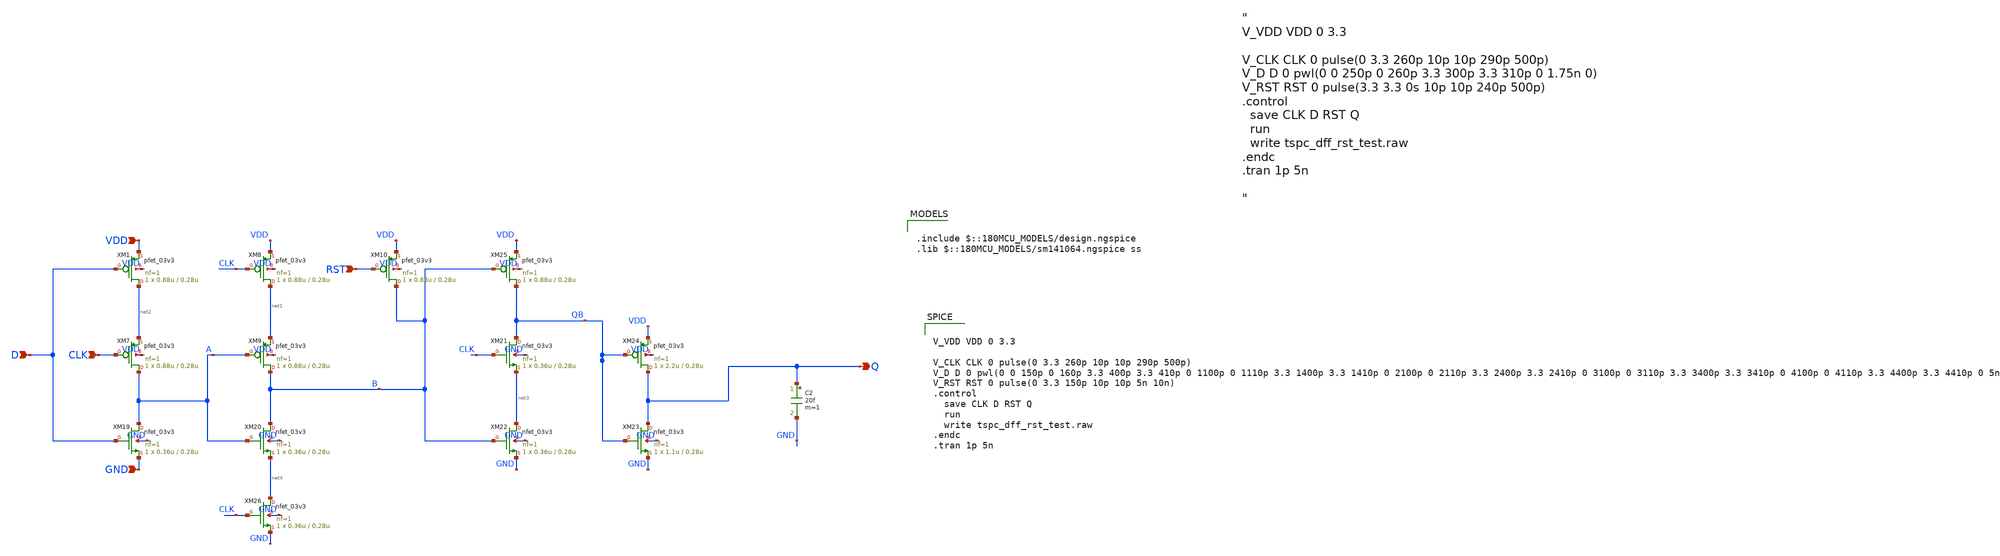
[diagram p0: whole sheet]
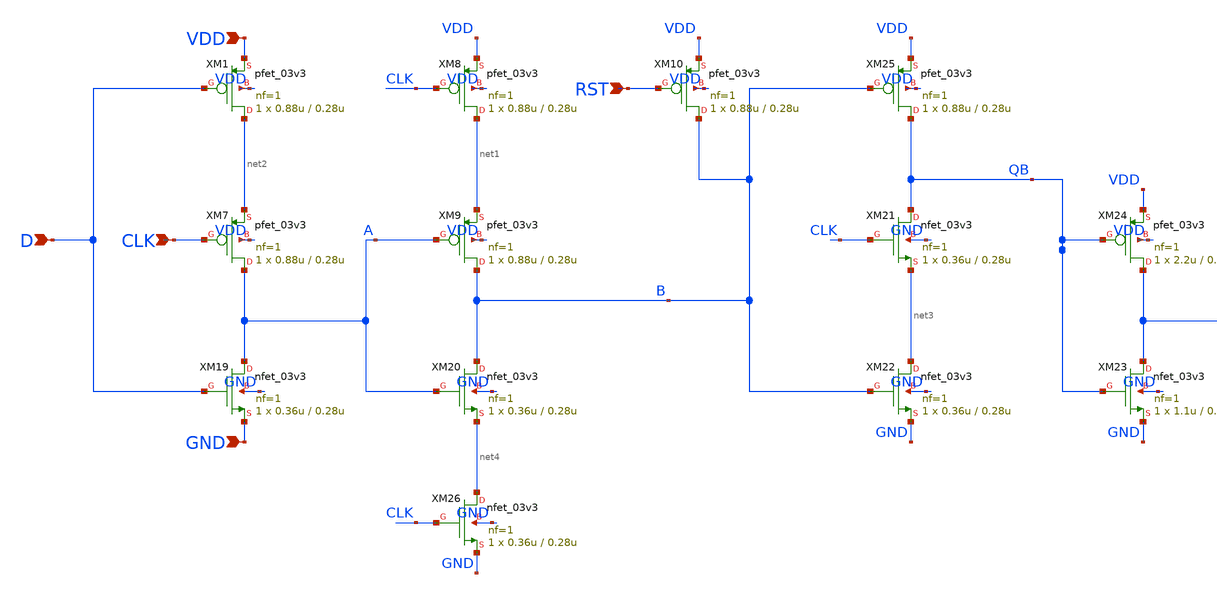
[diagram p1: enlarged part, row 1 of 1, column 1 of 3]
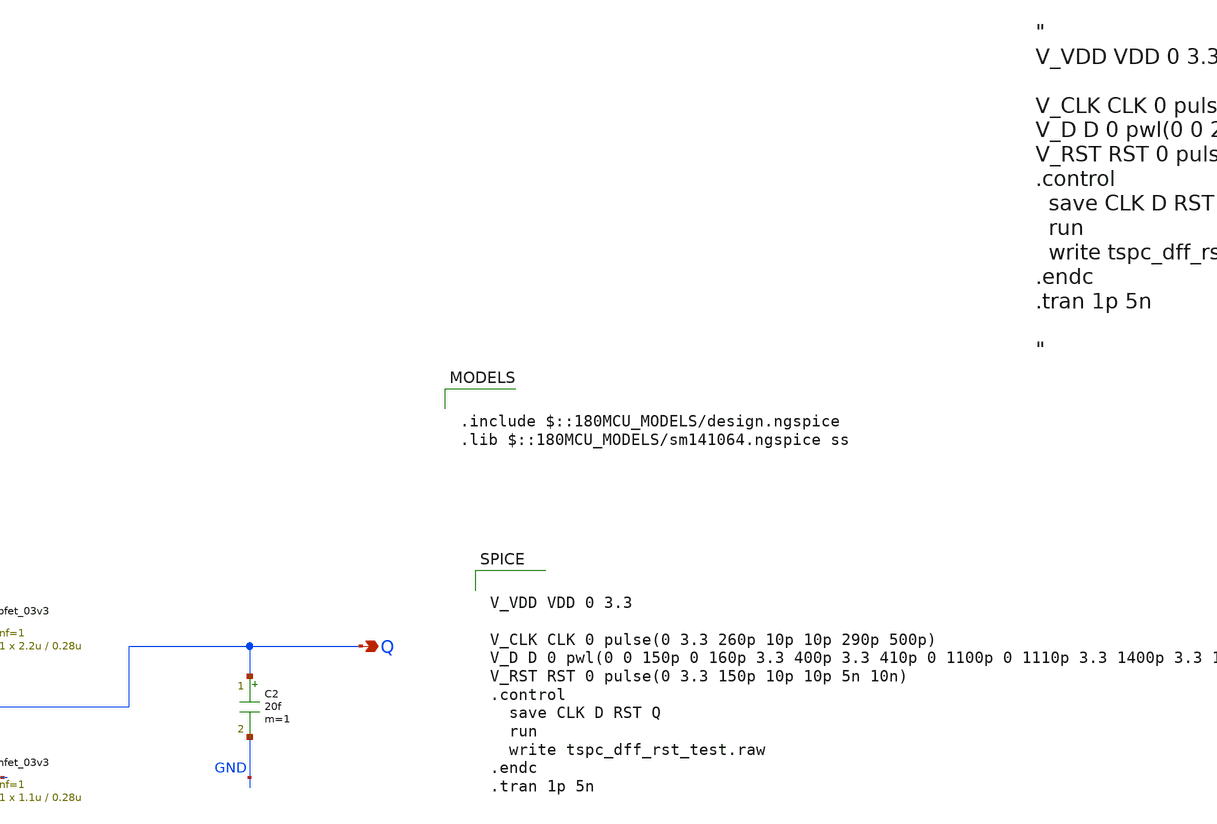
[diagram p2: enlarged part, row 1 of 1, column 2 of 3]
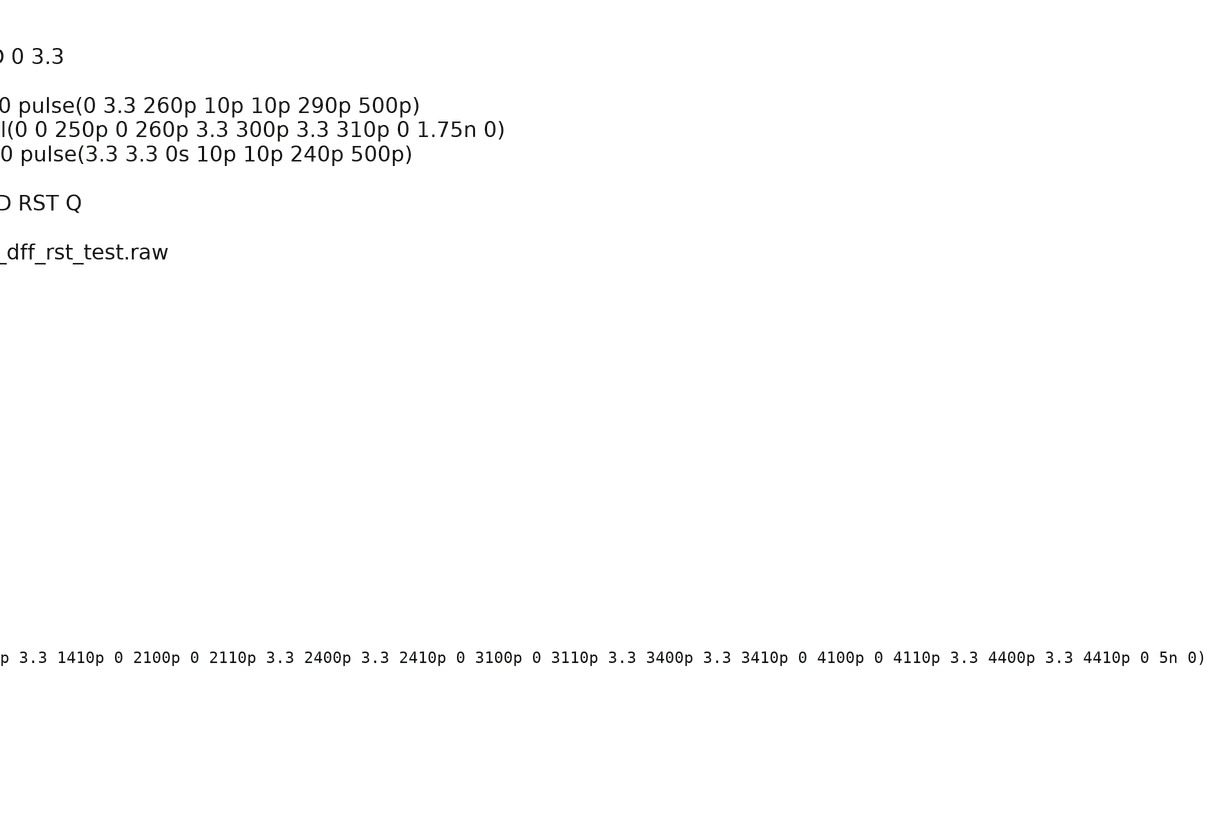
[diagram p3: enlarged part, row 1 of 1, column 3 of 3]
** sch_path: blocks/adc/encoder/tb/dff_test.sch
**.subckt dff_test Q D CLK RST VDD GND
*.opin Q
*.ipin D
*.ipin CLK
*.ipin RST
*.ipin VDD
*.ipin GND
C2 Q GND 20f m=1
XM1 net2 D VDD VDD pfet_03v3 L=0.28u W=0.88u nf=1 ad='int((nf+1)/2) * W/nf * 0.18u' as='int((nf+2)/2) * W/nf * 0.18u'
+ pd='2*int((nf+1)/2) * (W/nf + 0.18u)' ps='2*int((nf+2)/2) * (W/nf + 0.18u)' nrd='0.18u / W' nrs='0.18u / W'
+ sa=0 sb=0 sd=0 m=1
XM7 A CLK net2 VDD pfet_03v3 L=0.28u W=0.88u nf=1 ad='int((nf+1)/2) * W/nf * 0.18u' as='int((nf+2)/2) * W/nf * 0.18u'
+ pd='2*int((nf+1)/2) * (W/nf + 0.18u)' ps='2*int((nf+2)/2) * (W/nf + 0.18u)' nrd='0.18u / W' nrs='0.18u / W'
+ sa=0 sb=0 sd=0 m=1
XM8 net1 CLK VDD VDD pfet_03v3 L=0.28u W=0.88u nf=1 ad='int((nf+1)/2) * W/nf * 0.18u' as='int((nf+2)/2) * W/nf * 0.18u'
+ pd='2*int((nf+1)/2) * (W/nf + 0.18u)' ps='2*int((nf+2)/2) * (W/nf + 0.18u)' nrd='0.18u / W' nrs='0.18u / W'
+ sa=0 sb=0 sd=0 m=1
XM9 B A net1 VDD pfet_03v3 L=0.28u W=0.88u nf=1 ad='int((nf+1)/2) * W/nf * 0.18u' as='int((nf+2)/2) * W/nf * 0.18u'
+ pd='2*int((nf+1)/2) * (W/nf + 0.18u)' ps='2*int((nf+2)/2) * (W/nf + 0.18u)' nrd='0.18u / W' nrs='0.18u / W'
+ sa=0 sb=0 sd=0 m=1
XM10 B RST VDD VDD pfet_03v3 L=0.28u W=0.88u nf=1 ad='int((nf+1)/2) * W/nf * 0.18u' as='int((nf+2)/2) * W/nf * 0.18u'
+ pd='2*int((nf+1)/2) * (W/nf + 0.18u)' ps='2*int((nf+2)/2) * (W/nf + 0.18u)' nrd='0.18u / W' nrs='0.18u / W'
+ sa=0 sb=0 sd=0 m=1
XM19 A D GND GND nfet_03v3 L=0.28u W=0.36u nf=1 ad='int((nf+1)/2) * W/nf * 0.18u' as='int((nf+2)/2) * W/nf * 0.18u'
+ pd='2*int((nf+1)/2) * (W/nf + 0.18u)' ps='2*int((nf+2)/2) * (W/nf + 0.18u)' nrd='0.18u / W' nrs='0.18u / W'
+ sa=0 sb=0 sd=0 m=1
XM20 B A net4 GND nfet_03v3 L=0.28u W=0.36u nf=1 ad='int((nf+1)/2) * W/nf * 0.18u' as='int((nf+2)/2) * W/nf * 0.18u'
+ pd='2*int((nf+1)/2) * (W/nf + 0.18u)' ps='2*int((nf+2)/2) * (W/nf + 0.18u)' nrd='0.18u / W' nrs='0.18u / W'
+ sa=0 sb=0 sd=0 m=1
XM21 QB CLK net3 GND nfet_03v3 L=0.28u W=0.36u nf=1 ad='int((nf+1)/2) * W/nf * 0.18u' as='int((nf+2)/2) * W/nf * 0.18u'
+ pd='2*int((nf+1)/2) * (W/nf + 0.18u)' ps='2*int((nf+2)/2) * (W/nf + 0.18u)' nrd='0.18u / W' nrs='0.18u / W'
+ sa=0 sb=0 sd=0 m=1
XM22 net3 B GND GND nfet_03v3 L=0.28u W=0.36u nf=1 ad='int((nf+1)/2) * W/nf * 0.18u' as='int((nf+2)/2) * W/nf * 0.18u'
+ pd='2*int((nf+1)/2) * (W/nf + 0.18u)' ps='2*int((nf+2)/2) * (W/nf + 0.18u)' nrd='0.18u / W' nrs='0.18u / W'
+ sa=0 sb=0 sd=0 m=1
XM23 Q QB GND GND nfet_03v3 L=0.28u W=1.1u nf=1 ad='int((nf+1)/2) * W/nf * 0.18u' as='int((nf+2)/2) * W/nf * 0.18u'
+ pd='2*int((nf+1)/2) * (W/nf + 0.18u)' ps='2*int((nf+2)/2) * (W/nf + 0.18u)' nrd='0.18u / W' nrs='0.18u / W'
+ sa=0 sb=0 sd=0 m=1
XM24 Q QB VDD VDD pfet_03v3 L=0.28u W=2.2u nf=1 ad='int((nf+1)/2) * W/nf * 0.18u' as='int((nf+2)/2) * W/nf * 0.18u'
+ pd='2*int((nf+1)/2) * (W/nf + 0.18u)' ps='2*int((nf+2)/2) * (W/nf + 0.18u)' nrd='0.18u / W' nrs='0.18u / W'
+ sa=0 sb=0 sd=0 m=1
XM25 QB B VDD VDD pfet_03v3 L=0.28u W=0.88u nf=1 ad='int((nf+1)/2) * W/nf * 0.18u' as='int((nf+2)/2) * W/nf * 0.18u'
+ pd='2*int((nf+1)/2) * (W/nf + 0.18u)' ps='2*int((nf+2)/2) * (W/nf + 0.18u)' nrd='0.18u / W' nrs='0.18u / W'
+ sa=0 sb=0 sd=0 m=1
XM26 net4 CLK GND GND nfet_03v3 L=0.28u W=0.36u nf=1 ad='int((nf+1)/2) * W/nf * 0.18u' as='int((nf+2)/2) * W/nf * 0.18u'
+ pd='2*int((nf+1)/2) * (W/nf + 0.18u)' ps='2*int((nf+2)/2) * (W/nf + 0.18u)' nrd='0.18u / W' nrs='0.18u / W'
+ sa=0 sb=0 sd=0 m=1
**** begin user architecture code

.include $::180MCU_MODELS/design.ngspice
.lib $::180MCU_MODELS/sm141064.ngspice ss



V_VDD VDD 0 3.3

V_CLK CLK 0 pulse(0 3.3 260p 10p 10p 290p 500p)
V_D D 0 pwl(0 0 150p 0 160p 3.3 400p 3.3 410p 0 1100p 0 1110p 3.3 1400p 3.3 1410p 0 2100p 0 2110p
+ 3.3 2400p 3.3 2410p 0 3100p 0 3110p 3.3 3400p 3.3 3410p 0 4100p 0 4110p 3.3 4400p 3.3 4410p 0 5n 0)
V_RST RST 0 pulse(0 3.3 150p 10p 10p 5n 10n)
.control
  save CLK D RST Q
  run
  write tspc_dff_rst_test.raw
.endc
.tran 1p 5n



**** end user architecture code
**.ends
.end
